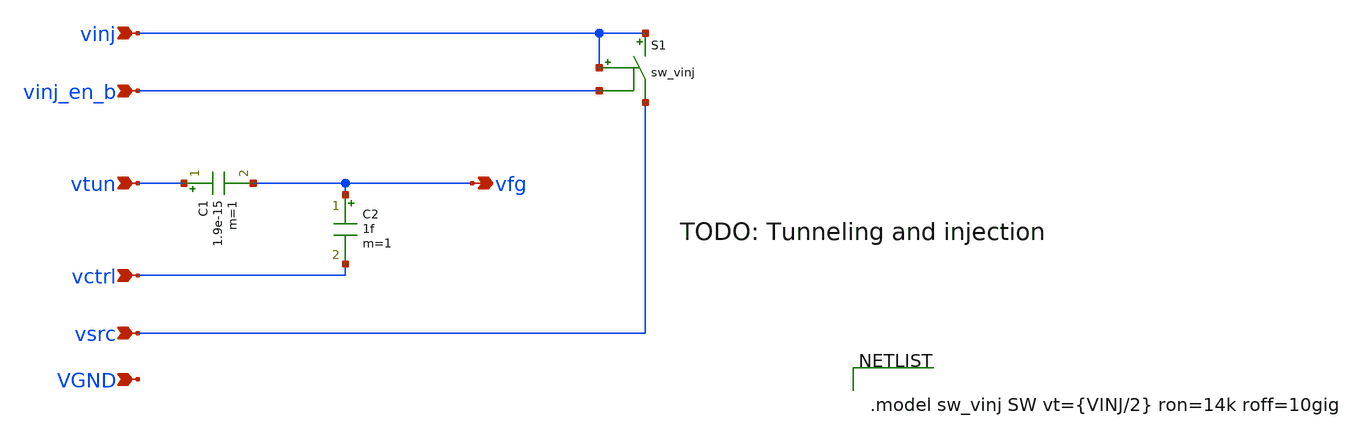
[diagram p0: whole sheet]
** sch_path: xschem/ideal_fgcell.sch
**.subckt ideal_fgcell vctrl vtun vinj vinj_en_b vsrc VGND vfg
*.ipin vctrl
*.ipin vtun
*.ipin vinj
*.ipin vinj_en_b
*.ipin vsrc
*.ipin VGND
*.opin vfg
C1 vtun vfg 1.9e-15 m=1
C2 vfg vctrl 1f m=1
S1 vinj vsrc vinj vinj_en_b sw_vinj
**** begin user architecture code


.model sw_vinj SW vt={VINJ/2} ron=14k roff=10gig


**** end user architecture code
**.ends
.end
